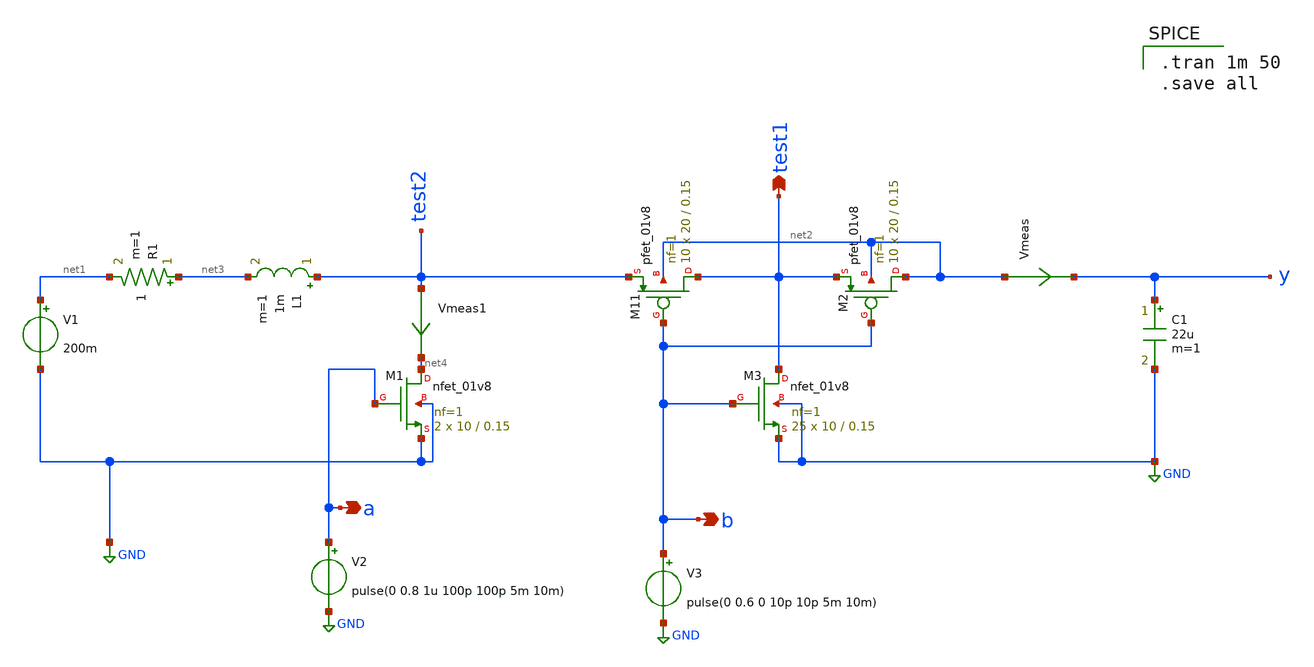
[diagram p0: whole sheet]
** sch_path: component/Core Functionality of boost Converter/vs test2.sch
**.subckt vs test2 a test1 b
*.opin a
*.opin test1
*.opin b
V1 net1 GND 200m
C1 y GND 22u m=1
L1 test2 net3 1m m=1
XM1 net4 a GND GND sky130_fd_pr__nfet_01v8 L=0.15 W=10 nf=1 ad='int((nf+1)/2) * W/nf * 0.29' as='int((nf+2)/2) * W/nf * 0.29'
+ pd='2*int((nf+1)/2) * (W/nf + 0.29)' ps='2*int((nf+2)/2) * (W/nf + 0.29)' nrd='0.29 / W' nrs='0.29 / W'
+ sa=0 sb=0 sd=0 mult=2 m=2
XM11 test1 b test2 net2 sky130_fd_pr__pfet_01v8 L=0.15 W=20 nf=1 ad='int((nf+1)/2) * W/nf * 0.29' as='int((nf+2)/2) * W/nf * 0.29'
+ pd='2*int((nf+1)/2) * (W/nf + 0.29)' ps='2*int((nf+2)/2) * (W/nf + 0.29)' nrd='0.29 / W' nrs='0.29 / W'
+ sa=0 sb=0 sd=0 mult=10 m=10
V2 a GND pulse(0 0.8 1u 100p 100p 5m 10m)
R1 net3 net1 1 m=1
Vmeas net2 y 0
.save i(vmeas)
Vmeas1 test2 net4 0
.save i(vmeas1)
XM2 net2 b test1 net2 sky130_fd_pr__pfet_01v8 L=0.15 W=20 nf=1 ad='int((nf+1)/2) * W/nf * 0.29' as='int((nf+2)/2) * W/nf * 0.29'
+ pd='2*int((nf+1)/2) * (W/nf + 0.29)' ps='2*int((nf+2)/2) * (W/nf + 0.29)' nrd='0.29 / W' nrs='0.29 / W'
+ sa=0 sb=0 sd=0 mult=10 m=10
XM3 test1 b GND GND sky130_fd_pr__nfet_01v8 L=0.15 W=10 nf=1 ad='int((nf+1)/2) * W/nf * 0.29' as='int((nf+2)/2) * W/nf * 0.29'
+ pd='2*int((nf+1)/2) * (W/nf + 0.29)' ps='2*int((nf+2)/2) * (W/nf + 0.29)' nrd='0.29 / W' nrs='0.29 / W'
+ sa=0 sb=0 sd=0 mult=25 m=25
V3 b GND pulse(0 0.6 0 10p 10p 5m 10m)
**** begin user architecture code

** opencircuitdesign pdks install
.lib $::SKYWATER_MODELS/sky130.lib.spice tt



.tran 1m 50
.save all

**** end user architecture code
**.ends
.GLOBAL GND
.end
